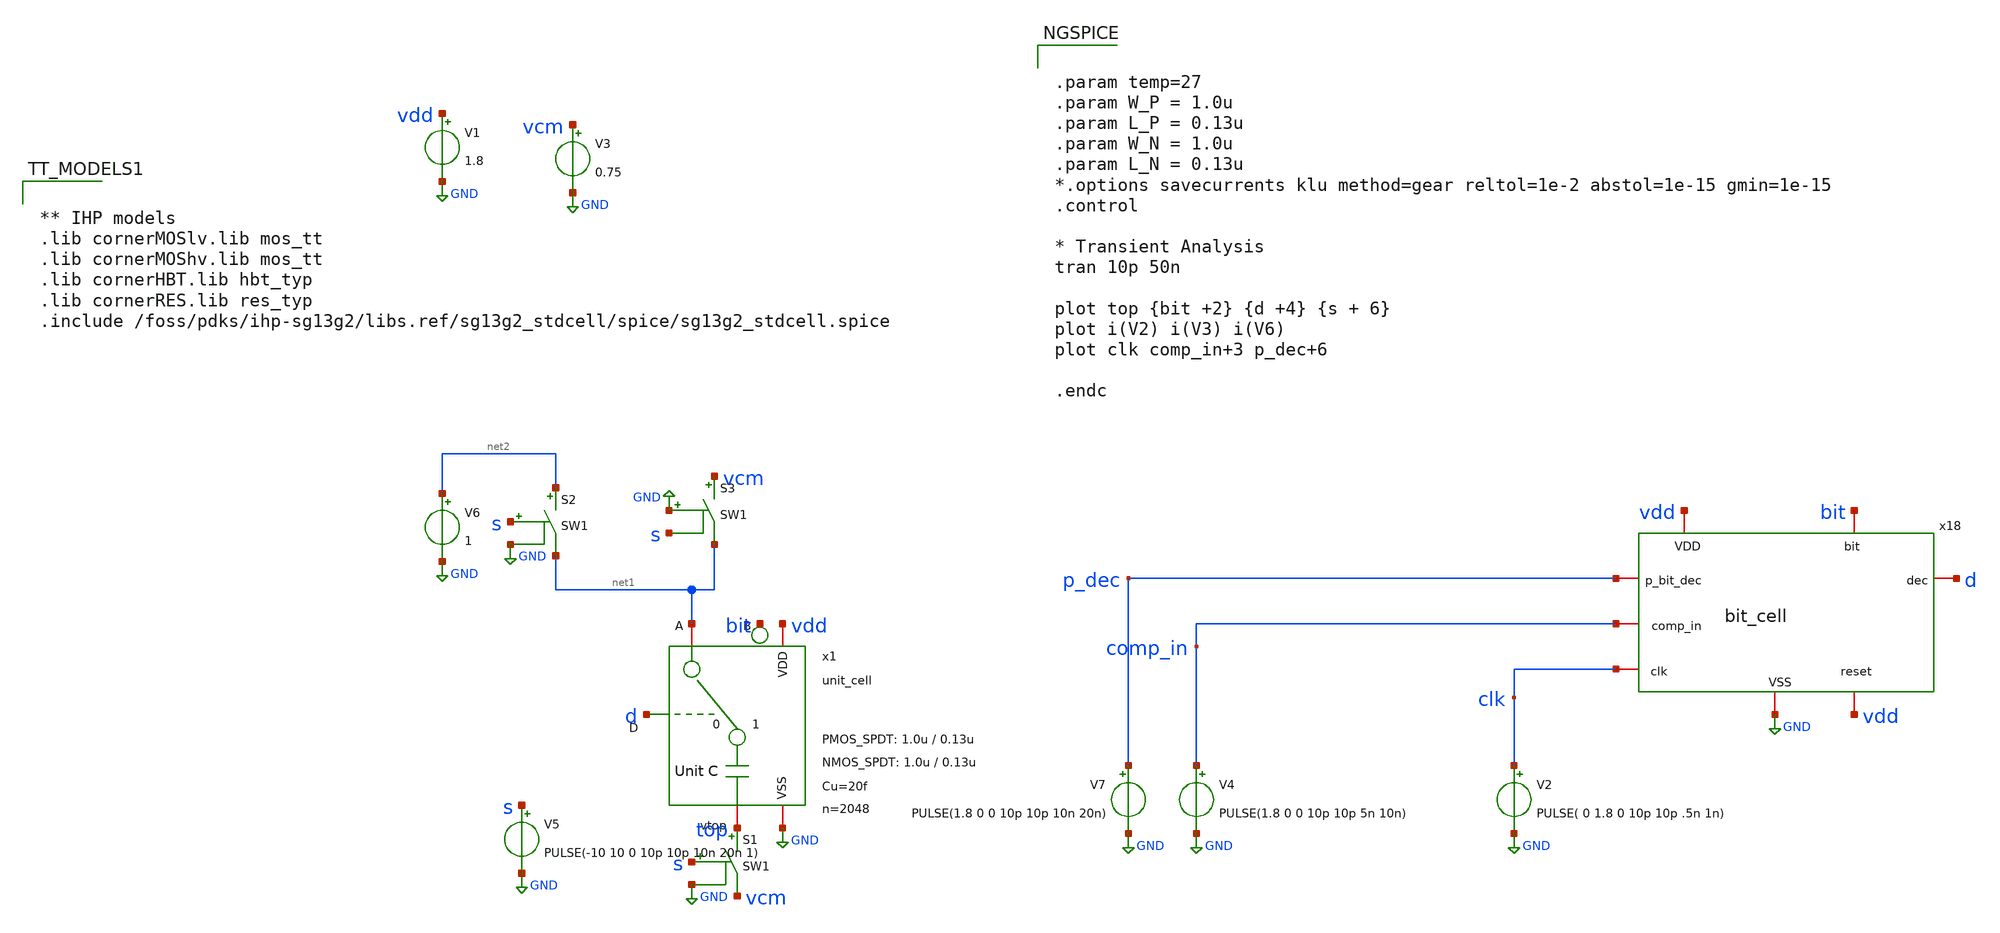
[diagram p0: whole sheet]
** sch_path: xschem/dac_icms_cell/testbenches/tb_unit_cell_logic_reg_tran.sch
**.subckt tb_unit_cell_logic_reg_tran
x1 bit net1 GND d vdd top unit_cell W_P_SPDT=1.0u L_P_SPDT=0.13u W_N_SPDT=1.0u L_N_SPDT=0.13u Cu=20f
+ n=2048
V1 vdd GND 1.8
V2 clk GND PULSE( 0 1.8 0 10p 10p .5n 1n)
V3 vcm GND 0.75
V4 comp_in GND PULSE(1.8 0 0 10p 10p 5n 10n)
S1 top vcm s GND SW1
V5 s GND PULSE(-10 10 0 10p 10p 10n 20n 1)
S2 net2 net1 s GND SW1
S3 vcm net1 GND s SW1
V6 net2 GND 1
x18 clk p_dec vdd comp_in vdd bit GND d bit_cell
V7 p_dec GND PULSE(1.8 0 0 10p 10p 10n 20n)
**** begin user architecture code


.param temp=27
.param W_P = 1.0u
.param L_P = 0.13u
.param W_N = 1.0u
.param L_N = 0.13u
*.options savecurrents klu method=gear reltol=1e-2 abstol=1e-15 gmin=1e-15
.control

* Transient Analysis
tran 10p 50n

plot top {bit +2} {d +4} {s + 6}
plot i(V2) i(V3) i(V6)
plot clk comp_in+3 p_dec+6

.endc




** IHP models
.lib cornerMOSlv.lib mos_tt
.lib cornerMOShv.lib mos_tt
.lib cornerHBT.lib hbt_typ
.lib cornerRES.lib res_typ
.include /foss/pdks/ihp-sg13g2/libs.ref/sg13g2_stdcell/spice/sg13g2_stdcell.spice


**** end user architecture code
**.ends
.GLOBAL GND
**** begin user architecture code
.MODEL SW1 SW   VT=0.9 VH=0.01  RON=10 ROFF=1G
**** end user architecture code
.end
